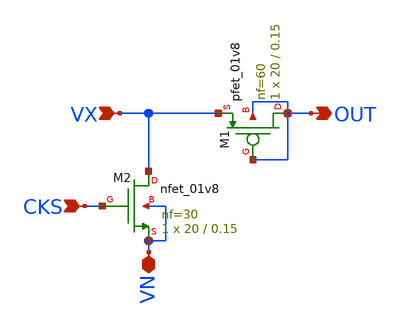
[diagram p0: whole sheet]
** sch_path: Layout/current111.sch
**.subckt current111 VN VX CKS OUT
*.iopin VN
*.ipin VX
*.ipin CKS
*.opin OUT
XM1 OUT OUT VX OUT sky130_fd_pr__pfet_01v8 L=0.15 W=20 nf=60 ad='int((nf+1)/2) * W/nf * 0.29' as='int((nf+2)/2) * W/nf * 0.29'
+ pd='2*int((nf+1)/2) * (W/nf + 0.29)' ps='2*int((nf+2)/2) * (W/nf + 0.29)' nrd='0.29 / W' nrs='0.29 / W'
+ sa=0 sb=0 sd=0 mult=1 m=1
XM2 VX CKS VN VN sky130_fd_pr__nfet_01v8 L=0.15 W=20 nf=30 ad='int((nf+1)/2) * W/nf * 0.29' as='int((nf+2)/2) * W/nf * 0.29'
+ pd='2*int((nf+1)/2) * (W/nf + 0.29)' ps='2*int((nf+2)/2) * (W/nf + 0.29)' nrd='0.29 / W' nrs='0.29 / W'
+ sa=0 sb=0 sd=0 mult=1 m=1
**.ends
.end
